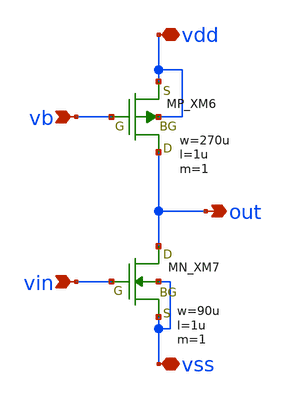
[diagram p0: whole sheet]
** sch_path: schematic/20250924_OSS_Workshop/ishikai/opamp/sample/cs.sch
**.subckt cs vb vin out vss vdd
*.ipin vb
*.ipin vin
*.opin out
*.iopin vss
*.iopin vdd
XM6 out vb vdd vdd PMOS w=270u l=1u as=0 ad=0 ps=0 pd=0 nrd=0 nrs=0 m=1
XM7 out vin vss vss NMOS w=90u l=1u as=0 ad=0 ps=0 pd=0 nrd=0 nrs=0 m=1
**.ends
.end
